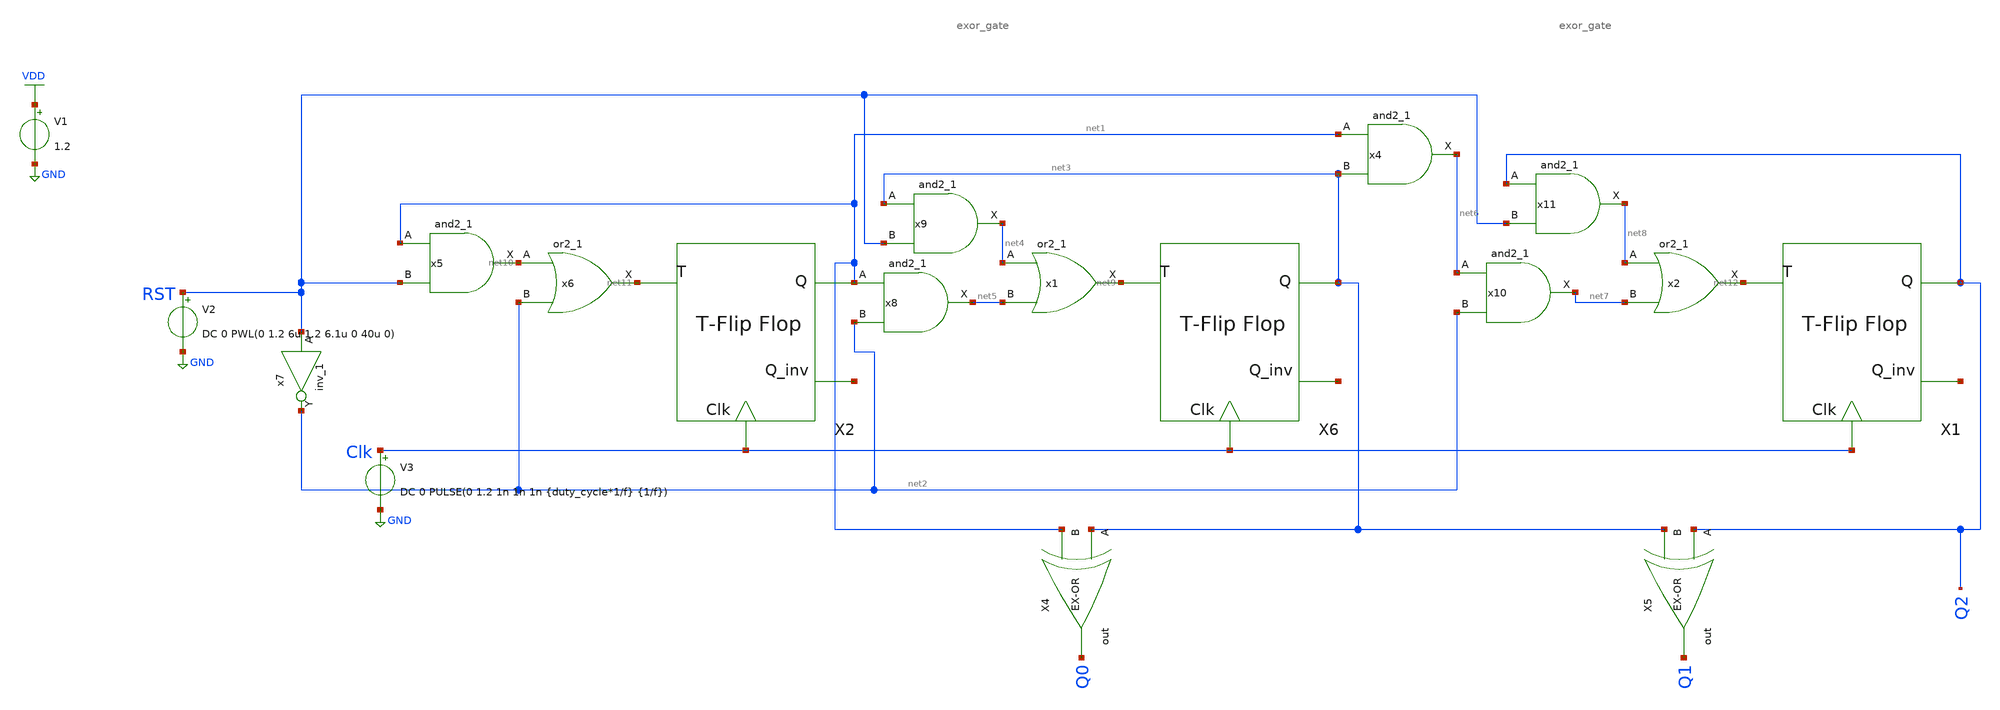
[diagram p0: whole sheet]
** sch_path: xschem/Reset_Counters/3_bit_rst_gray_counter_test.sch
**.subckt 3_bit_rst_gray_counter_test
x1 net4 net5 GND GND VDD VDD net9 sky130_fd_sc_lp__or2_1
x4 net1 net3 GND GND VDD VDD net6 sky130_fd_sc_lp__and2_1
x5 net1 RST GND GND VDD VDD net10 sky130_fd_sc_lp__and2_1
x6 net10 net2 GND GND VDD VDD net11 sky130_fd_sc_lp__or2_1
x7 RST GND GND VDD VDD net2 sky130_fd_sc_lp__inv_1
x8 net1 net2 GND GND VDD VDD net5 sky130_fd_sc_lp__and2_1
x9 net3 RST GND GND VDD VDD net4 sky130_fd_sc_lp__and2_1
x10 net6 net2 GND GND VDD VDD net7 sky130_fd_sc_lp__and2_1
x11 Q2 RST GND GND VDD VDD net8 sky130_fd_sc_lp__and2_1
x2 net8 net7 GND GND VDD VDD net12 sky130_fd_sc_lp__or2_1
V1 VDD GND 1.2
V3 Clk GND DC 0 PULSE(0 1.2 1n 1n 1n {duty_cycle*1/f} {1/f})
V2 RST GND DC 0 PWL(0 1.2 6u 1.2 6.1u 0 40u 0)
X4 net3 net1 Q0 exor_gate
X5 Q2 net3 Q1 exor_gate
X6 net9 net3 net13 Clk T_flip_flop
X1 net12 Q2 net14 Clk T_flip_flop
X2 net11 net1 net15 Clk T_flip_flop
**** begin user architecture code


.lib /home/sky/sky130A/libs.tech/ngspice/sky130.lib.spice tt
.include /home/sky/sky130A/libs.ref/sky130_fd_sc_lp/spice/sky130_fd_sc_lp.spice
.options abstol=1e-14 reltol=1e-4
.param f=2560k
.param duty_cycle=0.5
*.ic v(Q)=0 v(Q_inv)=1 v(x1.net1)=0
.tran {(1/100)*(1/f)} {40/f}
.save all


**** end user architecture code
**.ends

* expanding   symbol:  exor_gate/exor_gate.sym # of pins=3
** sym_path: xschem/exor_gate/exor_gate.sym
** sch_path: xschem/exor_gate/exor_gate.sch
.subckt exor_gate A B out
*.ipin A
*.ipin B
*.opin out
XM4 out A net1 GND sky130_fd_pr__nfet_01v8 L=0.18 W=0.5 nf=1 ad='int((nf+1)/2) * W/nf * 0.29' as='int((nf+2)/2) * W/nf * 0.29'
+ pd='2*int((nf+1)/2) * (W/nf + 0.29)' ps='2*int((nf+2)/2) * (W/nf + 0.29)' nrd='0.29 / W' nrs='0.29 / W'
+ sa=0 sb=0 sd=0 mult=1 m=1
XM5 net3 B VDD VDD sky130_fd_pr__pfet_01v8 L=0.18 W=1 nf=1 ad='int((nf+1)/2) * W/nf * 0.29' as='int((nf+2)/2) * W/nf * 0.29'
+ pd='2*int((nf+1)/2) * (W/nf + 0.29)' ps='2*int((nf+2)/2) * (W/nf + 0.29)' nrd='0.29 / W' nrs='0.29 / W'
+ sa=0 sb=0 sd=0 mult=1 m=1
XM1 net1 B GND GND sky130_fd_pr__nfet_01v8 L=0.18 W=0.5 nf=1 ad='int((nf+1)/2) * W/nf * 0.29' as='int((nf+2)/2) * W/nf * 0.29'
+ pd='2*int((nf+1)/2) * (W/nf + 0.29)' ps='2*int((nf+2)/2) * (W/nf + 0.29)' nrd='0.29 / W' nrs='0.29 / W'
+ sa=0 sb=0 sd=0 mult=1 m=1
XM2 out net5 net3 VDD sky130_fd_pr__pfet_01v8 L=0.18 W=1 nf=1 ad='int((nf+1)/2) * W/nf * 0.29' as='int((nf+2)/2) * W/nf * 0.29'
+ pd='2*int((nf+1)/2) * (W/nf + 0.29)' ps='2*int((nf+2)/2) * (W/nf + 0.29)' nrd='0.29 / W' nrs='0.29 / W'
+ sa=0 sb=0 sd=0 mult=1 m=1
XM3 net4 net6 VDD VDD sky130_fd_pr__pfet_01v8 L=0.18 W=1 nf=1 ad='int((nf+1)/2) * W/nf * 0.29' as='int((nf+2)/2) * W/nf * 0.29'
+ pd='2*int((nf+1)/2) * (W/nf + 0.29)' ps='2*int((nf+2)/2) * (W/nf + 0.29)' nrd='0.29 / W' nrs='0.29 / W'
+ sa=0 sb=0 sd=0 mult=1 m=1
XM6 out A net4 VDD sky130_fd_pr__pfet_01v8 L=0.18 W=1 nf=1 ad='int((nf+1)/2) * W/nf * 0.29' as='int((nf+2)/2) * W/nf * 0.29'
+ pd='2*int((nf+1)/2) * (W/nf + 0.29)' ps='2*int((nf+2)/2) * (W/nf + 0.29)' nrd='0.29 / W' nrs='0.29 / W'
+ sa=0 sb=0 sd=0 mult=1 m=1
XM7 out net5 net2 GND sky130_fd_pr__nfet_01v8 L=0.18 W=0.5 nf=1 ad='int((nf+1)/2) * W/nf * 0.29' as='int((nf+2)/2) * W/nf * 0.29'
+ pd='2*int((nf+1)/2) * (W/nf + 0.29)' ps='2*int((nf+2)/2) * (W/nf + 0.29)' nrd='0.29 / W' nrs='0.29 / W'
+ sa=0 sb=0 sd=0 mult=1 m=1
XM8 net2 net6 GND GND sky130_fd_pr__nfet_01v8 L=0.18 W=0.5 nf=1 ad='int((nf+1)/2) * W/nf * 0.29' as='int((nf+2)/2) * W/nf * 0.29'
+ pd='2*int((nf+1)/2) * (W/nf + 0.29)' ps='2*int((nf+2)/2) * (W/nf + 0.29)' nrd='0.29 / W' nrs='0.29 / W'
+ sa=0 sb=0 sd=0 mult=1 m=1
X3 B net6 inv Wpmos=3 Lpmos=0.18 Wnmos=1 Lnmos=0.18
X2 A net5 inv Wpmos=3 Lpmos=0.18 Wnmos=1 Lnmos=0.18
.ends


* expanding   symbol:  T_flip_flop/T_flip_flop.sym # of pins=4
** sym_path: xschem/T_flip_flop/T_flip_flop.sym
** sch_path: xschem/T_flip_flop/T_flip_flop.sch
.subckt T_flip_flop T Q Q_inv Clk
*.ipin T
*.ipin Clk
*.opin Q
*.opin Q_inv
X1 net1 Q Q_inv Clk d_flip_flop
X2 Q T net1 exor_gate
.ends


* expanding   symbol:  inv/inv.sym # of pins=2
** sym_path: xschem/inv/inv.sym
** sch_path: xschem/inv/inv.sch
.subckt inv in out  Wpmos=3 Lpmos=0.18 Wnmos=1 Lnmos=0.18
*.ipin in
*.iopin out
XM1 out in GND GND sky130_fd_pr__nfet_01v8 L=Lnmos W=Wnmos nf=1 ad='int((nf+1)/2) * W/nf * 0.29' as='int((nf+2)/2) * W/nf * 0.29'
+ pd='2*int((nf+1)/2) * (W/nf + 0.29)' ps='2*int((nf+2)/2) * (W/nf + 0.29)' nrd='0.29 / W' nrs='0.29 / W'
+ sa=0 sb=0 sd=0 mult=1 m=1
XM2 out in VDD VDD sky130_fd_pr__pfet_01v8 L=Lpmos W=Wpmos nf=1 ad='int((nf+1)/2) * W/nf * 0.29' as='int((nf+2)/2) * W/nf * 0.29'
+ pd='2*int((nf+1)/2) * (W/nf + 0.29)' ps='2*int((nf+2)/2) * (W/nf + 0.29)' nrd='0.29 / W' nrs='0.29 / W'
+ sa=0 sb=0 sd=0 mult=1 m=1
.ends


* expanding   symbol:  D_flip_flop/d_flip_flop.sym # of pins=4
** sym_path: xschem/D_flip_flop/d_flip_flop.sym
** sch_path: xschem/D_flip_flop/d_flip_flop.sch
.subckt d_flip_flop D Q Q_inv Clk
*.ipin D
*.ipin Clk
*.opin Q_inv
*.opin Q
X1 net1 net2 inv Wpmos=3 Lpmos=0.18 Wnmos=1 Lnmos=0.18
X2 net3 Q inv Wpmos=3 Lpmos=0.18 Wnmos=1 Lnmos=0.18
X3 net2 net4 inv Wpmos=3 Lpmos=0.18 Wnmos=1 Lnmos=0.18
X4 Q Q_inv inv Wpmos=3 Lpmos=0.18 Wnmos=1 Lnmos=0.18
X5 D net1 Clk Clk_inv transmission_gate Wpmos=1 Lpmos=0.18 Wnmos=1 Lnmos=0.18
X6 net1 net4 Clk_inv Clk transmission_gate Wpmos=1 Lpmos=0.18 Wnmos=1 Lnmos=0.18
X7 net3 Q_inv Clk Clk_inv transmission_gate Wpmos=1 Lpmos=0.18 Wnmos=1 Lnmos=0.18
X8 net2 net3 Clk_inv Clk transmission_gate Wpmos=1 Lpmos=0.18 Wnmos=1 Lnmos=0.18
X9 Clk Clk_inv inv Wpmos=3 Lpmos=0.18 Wnmos=1 Lnmos=0.18
.ends


* expanding   symbol:  transmission_gate/transmission_gate.sym # of pins=4
** sym_path: xschem/transmission_gate/transmission_gate.sym
** sch_path: xschem/transmission_gate/transmission_gate.sch
.subckt transmission_gate in out ctrl_ ctrl  Wpmos=1 Lpmos=0.18 Wnmos=1 Lnmos=0.18
*.iopin in
*.iopin out
*.ipin ctrl_
*.ipin ctrl
XM1 in ctrl out GND sky130_fd_pr__nfet_01v8 L=Lnmos W=Wnmos nf=1 ad='int((nf+1)/2) * W/nf * 0.29' as='int((nf+2)/2) * W/nf * 0.29'
+ pd='2*int((nf+1)/2) * (W/nf + 0.29)' ps='2*int((nf+2)/2) * (W/nf + 0.29)' nrd='0.29 / W' nrs='0.29 / W'
+ sa=0 sb=0 sd=0 mult=1 m=1
XM2 out ctrl_ in VDD sky130_fd_pr__pfet_01v8 L=Lpmos W=Wpmos nf=1 ad='int((nf+1)/2) * W/nf * 0.29' as='int((nf+2)/2) * W/nf * 0.29'
+ pd='2*int((nf+1)/2) * (W/nf + 0.29)' ps='2*int((nf+2)/2) * (W/nf + 0.29)' nrd='0.29 / W' nrs='0.29 / W'
+ sa=0 sb=0 sd=0 mult=1 m=1
.ends

.GLOBAL VDD
.GLOBAL GND
.end
